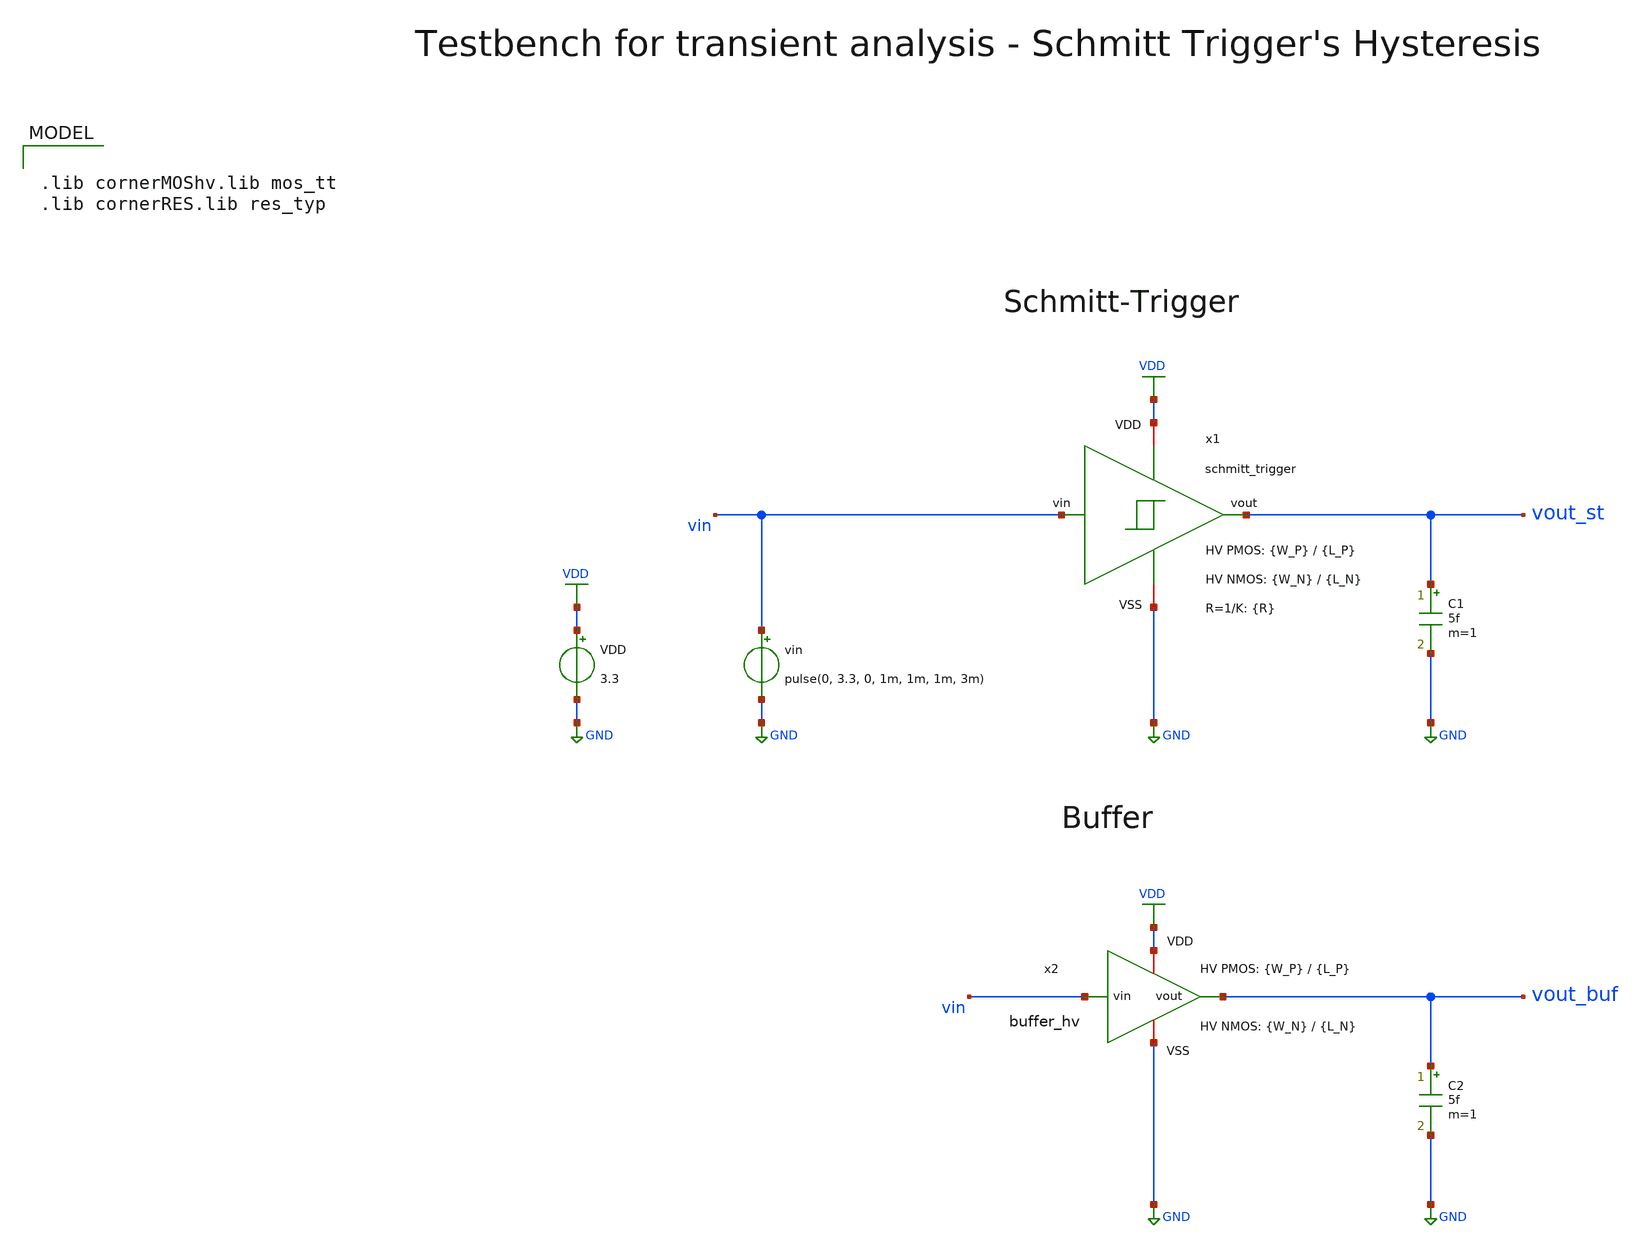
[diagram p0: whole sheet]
** sch_path: SG13G2_ATBS-ADC-main/xschem/schmitt_trigger/testbenches/schmitt_trigger_tb_tran.sch
**.subckt schmitt_trigger_tb_tran
C1 vout_st GND 5f m=1
vin vin GND pulse(0, 3.3, 0, 1m, 1m, 1m, 3m)
VDD VDD GND 3.3
C2 vout_buf GND 5f m=1
x1 VDD vout_st vin GND schmitt_trigger W_P_ST={W_P} L_P_ST={L_P} W_N_ST={W_N} L_N_ST={L_N} R={R}
x2 VDD vin vout_buf GND buffer_hv W_P_INV={W_P} L_P_INV={L_P} W_N_INV={W_N} L_N_INV={L_N}
**** begin user architecture code


.param temp=27
.param W_N=1u
.param L_N=0.5u
.param W_P=3u
.param L_P=0.5u
.param R=4
.options savecurrents reltol=1e-3 abstol=1e-12 gmin=1e-15
.control

save all

* Operating Point Analysis
op
remzerovec
write schmitt_trigger_tb_tran.raw
set appendwrite

* Transient Analysis
tran 5u 3ms
write schmitt_trigger_tb_tran.raw

* Measurements
meas tran cross_time1 find time WHEN vin = vout_st TD=0.1m
meas tran y_value1 find vin WHEN time = cross_time1

meas tran cross_time2 find time WHEN vin = vout_st TD=2.1m
meas tran y_value2 find vin WHEN time = cross_time2

let VH = y_value1 - y_value2
print VH

* Plotting
plot v(vin) v(vout_buf)
plot v(vin) v(vout_st)

* Writing Data
set wr_singlescale
set wr_vecnames
wrdata /foss/designs/SG13G2_ATBS-ADC-main/python/plot_simulations/data/schmitt_trigger_tb_tran.txt
+ v(vin) v(vout_buf) v(vout_st)

*quit
.endc


.lib cornerMOShv.lib mos_tt
.lib cornerRES.lib res_typ

**** end user architecture code
**.ends

* expanding   symbol:  schmitt_trigger/schmitt_trigger.sym # of pins=4
** sym_path: SG13G2_ATBS-ADC-main/xschem/schmitt_trigger/schmitt_trigger.sym
** sch_path: SG13G2_ATBS-ADC-main/xschem/schmitt_trigger/schmitt_trigger.sch
.subckt schmitt_trigger VDD vout vin VSS  W_P_ST=3.0u L_P_ST=0.50u W_N_ST=1.0u L_N_ST=0.50u R=4
*.iopin VDD
*.opin vout
*.iopin VSS
*.ipin vin
x1 VDD net2 vout VSS inverter_hv W_P=W_P_ST L_P=L_P_ST W_N=W_N_ST L_N=L_N_ST
XM5 net3 vin VDD VDD sg13_hv_pmos w=W_P_ST l=L_P_ST ng=1 m=1 mm_ok=1
XM4 net2 vin net3 VDD sg13_hv_pmos w=W_P_ST l=L_P_ST ng=1 m=1 mm_ok=1
XM6 VSS net2 net3 VDD sg13_hv_pmos w=R*W_P_ST l=L_P_ST ng=1 m=1 mm_ok=1
XM1 net1 vin VSS VSS sg13_hv_nmos w=W_N_ST l=L_N_ST ng=1 m=1 mm_ok=1
XM2 net2 vin net1 VSS sg13_hv_nmos w=W_N_ST l=L_N_ST ng=1 m=1 mm_ok=1
XM3 VDD net2 net1 VSS sg13_hv_nmos w=R*W_N_ST l=L_N_ST ng=1 m=1 mm_ok=1
.ends


* expanding   symbol:  buffer/buffer_hv.sym # of pins=4
** sym_path: SG13G2_ATBS-ADC-main/xschem/buffer/buffer_hv.sym
** sch_path: SG13G2_ATBS-ADC-main/xschem/buffer/buffer_hv.sch
.subckt buffer_hv VDD vin vout VSS  W_P_INV=3.0u L_P_INV=0.50u W_N_INV=1.0u L_N_INV=0.50u
*.ipin vin
*.iopin VDD
*.iopin VSS
*.opin vout
x1 VDD vin net1 VSS inverter_hv W_P=W_P_INV L_P=L_P_INV W_N=W_N_INV L_N=L_N_INV
x2 VDD net1 vout VSS inverter_hv W_P=W_P_INV L_P=L_P_INV W_N=W_N_INV L_N=L_N_INV
.ends


* expanding   symbol:  inverter/inverter_hv.sym # of pins=4
** sym_path: SG13G2_ATBS-ADC-main/xschem/inverter/inverter_hv.sym
** sch_path: SG13G2_ATBS-ADC-main/xschem/inverter/inverter_hv.sch
.subckt inverter_hv VDD vin vout VSS  W_P=3.0u L_P=0.50u W_N=1.0u L_N=0.50u
*.ipin vin
*.iopin VDD
*.iopin VSS
*.opin vout
XM1 vout vin VDD VDD sg13_hv_pmos w=W_P l=L_P ng=1 m=1 mm_ok=1
XM2 vout vin VSS VSS sg13_hv_nmos w=W_N l=L_N ng=1 m=1 mm_ok=1
.ends

.GLOBAL VDD
.GLOBAL GND
.end
